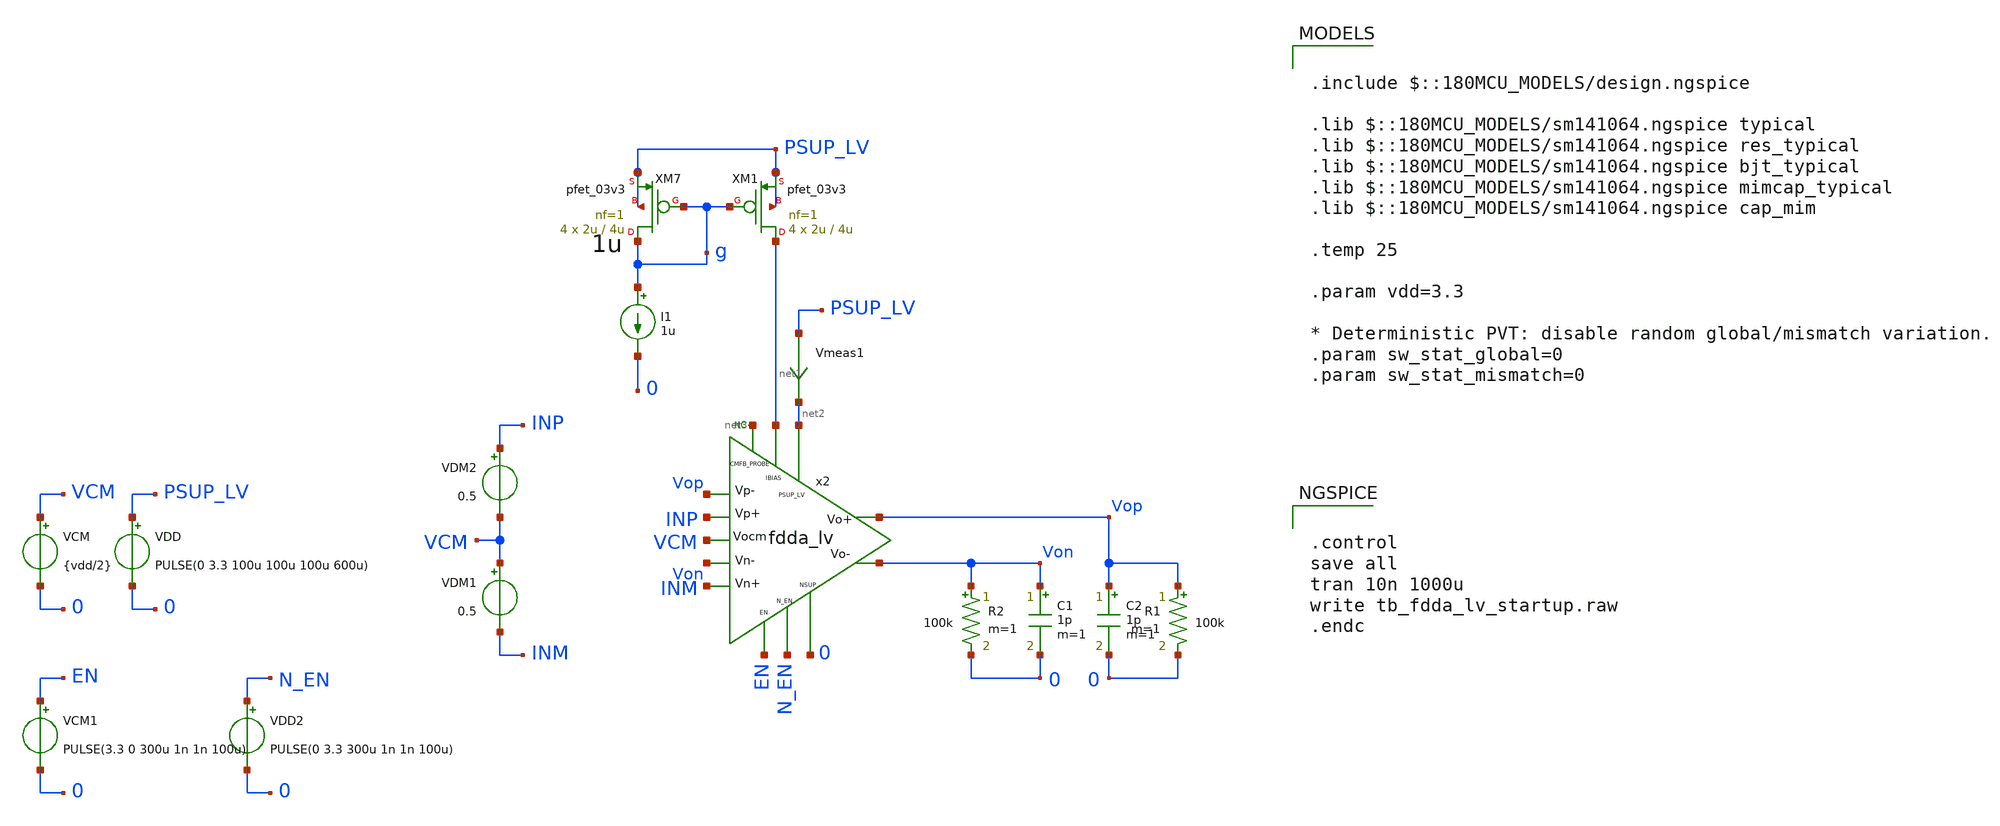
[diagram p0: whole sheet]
** sch_path: xschem/blocks/fdda_lv/tb_fdda_lv_startup.sch
**.subckt tb_fdda_lv_startup
C1 Von 0 1p m=1
x2 net2 Vop Von INM INP Vop Von net1 N_EN EN 0 net3 VCM fdda_lv
VDD PSUP_LV 0 PULSE(0 3.3 100u 100u 100u 600u)
C2 Vop 0 1p m=1
VCM VCM 0 {vdd/2}
VDM2 INP VCM 0.5
VDM1 VCM INM 0.5
* noconn #net3
XM7 g g PSUP_LV PSUP_LV pfet_03v3 L=4u W=2u nf=1 ad='int((nf+1)/2) * W/nf * 0.18u' as='int((nf+2)/2) * W/nf * 0.18u'
+ pd='2*int((nf+1)/2) * (W/nf + 0.18u)' ps='2*int((nf+2)/2) * (W/nf + 0.18u)' nrd='0.18u / W' nrs='0.18u / W'
+ sa=0 sb=0 sd=0 m=4
XM1 net1 g PSUP_LV PSUP_LV pfet_03v3 L=4u W=2u nf=1 ad='int((nf+1)/2) * W/nf * 0.18u' as='int((nf+2)/2) * W/nf * 0.18u'
+ pd='2*int((nf+1)/2) * (W/nf + 0.18u)' ps='2*int((nf+2)/2) * (W/nf + 0.18u)' nrd='0.18u / W' nrs='0.18u / W'
+ sa=0 sb=0 sd=0 m=4
I1 g 0 1u
VCM1 EN 0 PULSE(3.3 0 300u 1n 1n 100u)
VDD2 N_EN 0 PULSE(0 3.3 300u 1n 1n 100u)
Vmeas1 PSUP_LV net2 0
.save i(vmeas1)
R1 Vop 0 100k m=1
R2 Von 0 100k m=1
**** begin user architecture code

.include $::180MCU_MODELS/design.ngspice

.lib $::180MCU_MODELS/sm141064.ngspice typical
.lib $::180MCU_MODELS/sm141064.ngspice res_typical
.lib $::180MCU_MODELS/sm141064.ngspice bjt_typical
.lib $::180MCU_MODELS/sm141064.ngspice mimcap_typical
.lib $::180MCU_MODELS/sm141064.ngspice cap_mim

.temp 25

.param vdd=3.3

* Deterministic PVT: disable random global/mismatch variation.
.param sw_stat_global=0
.param sw_stat_mismatch=0



.control
save all
tran 10n 1000u
write tb_fdda_lv_startup.raw
.endc


**** end user architecture code
**.ends
.end
